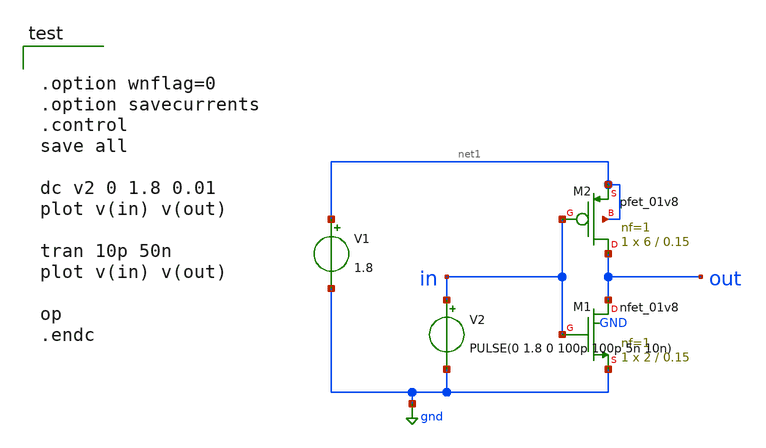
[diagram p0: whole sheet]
** sch_path: cmos_inv.sch
**.subckt cmos_inv
XM1 out in gnd GND sky130_fd_pr__nfet_01v8 L=0.15 W=2 nf=1 ad='int((1 + 1)/2) * 2 / 1 * 0.29' as='int((1 + 2)/2) * 2 / 1 * 0.29'
+ pd='2*int((1 + 1)/2) * (2 / 1 + 0.29)' ps='2*int((1 + 2)/2) * (2 / 1 + 0.29)' nrd='0.29 / 2 ' nrs='0.29 / 2 '
+ sa=0 sb=0 sd=0 mult=1 m=1
XM2 out in net1 net1 sky130_fd_pr__pfet_01v8 L=0.15 W=6 nf=1 ad='int((1 + 1)/2) * 6 / 1 * 0.29' as='int((1 + 2)/2) * 6 / 1 * 0.29'
+ pd='2*int((1 + 1)/2) * (6 / 1 + 0.29)' ps='2*int((1 + 2)/2) * (6 / 1 + 0.29)' nrd='0.29 / 6 ' nrs='0.29 / 6 '
+ sa=0 sb=0 sd=0 mult=1 m=1
V1 net1 gnd 1.8
V2 in gnd PULSE(0 1.8 0 100p 100p 5n 10n)
**** begin user architecture code

** opencircuitdesign pdks install
.lib $::SKYWATER_MODELS/sky130.lib.spice tt
.param mc_mm_switch=0
.param mc_pr_switch=1



.option wnflag=0
.option savecurrents
.control
save all

dc v2 0 1.8 0.01
plot v(in) v(out)

tran 10p 50n
plot v(in) v(out)

op
.endc


**** end user architecture code
**.ends
.GLOBAL gnd
.end
